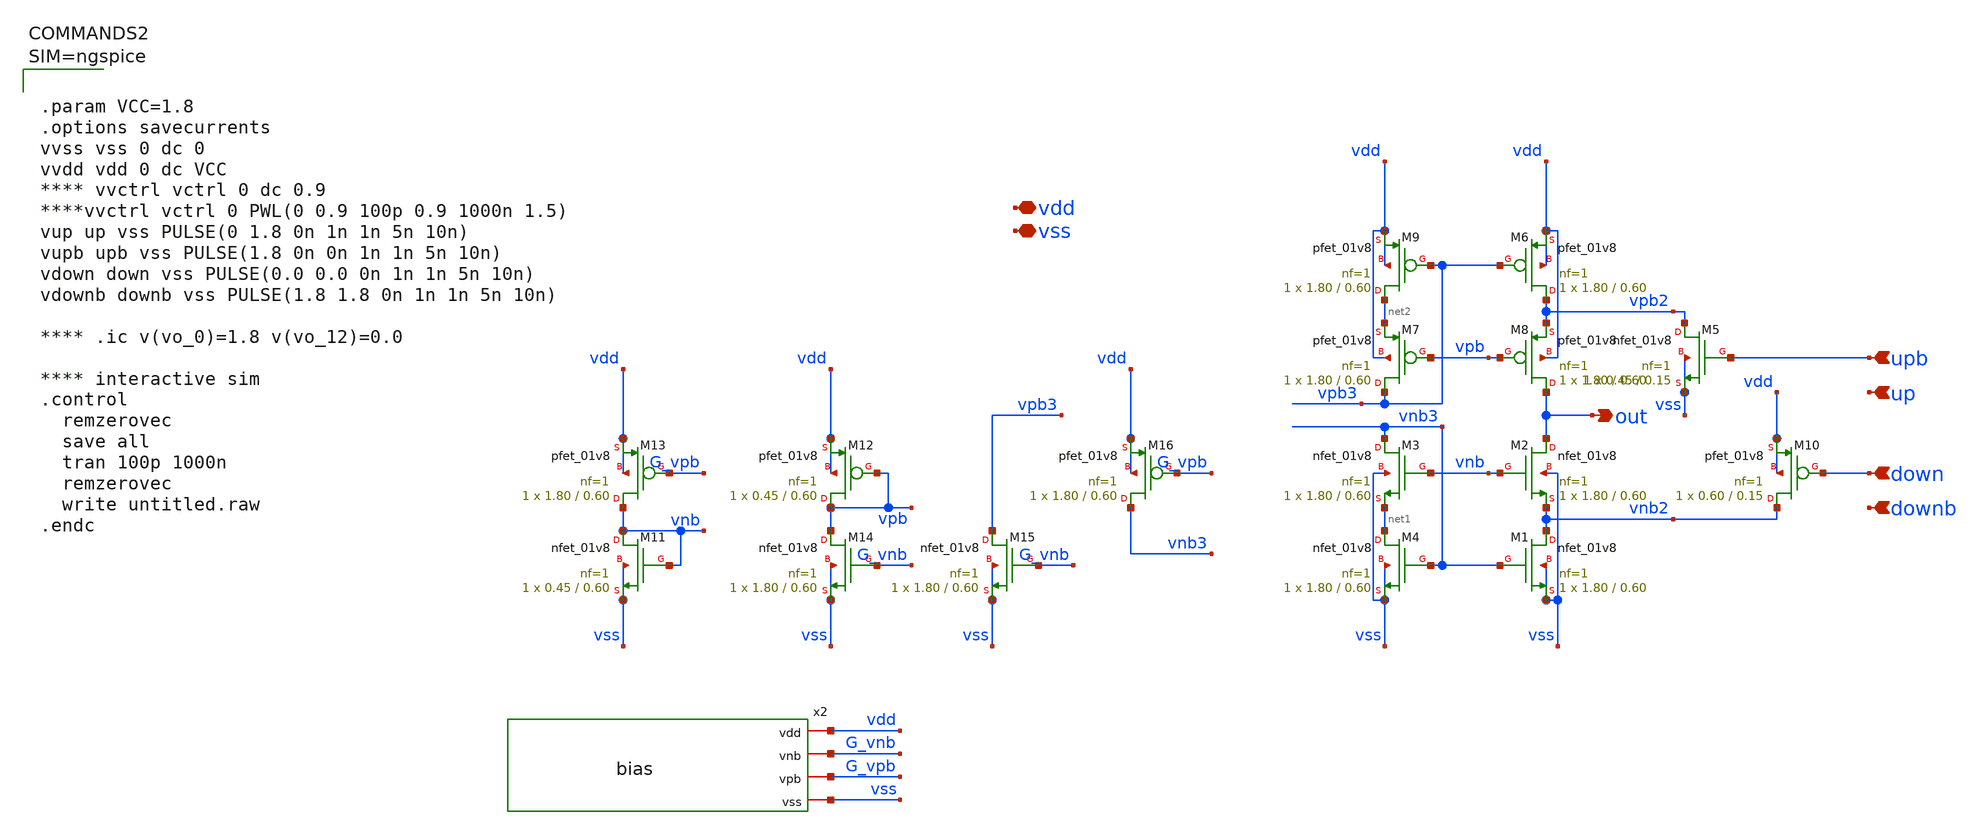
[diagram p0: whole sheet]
** sch_path: custom_gds/tt_um_mickey_pll/xschem/cp7.sch
.lib $::SKYWATER_MODELS/sky130.lib.spice tt
.include $::SKYWATER_STDCELLS/sky130_fd_sc_hd.spice

**.subckt cp7 upb up down downb out vdd vss
*.ipin upb
*.ipin up
*.ipin down
*.ipin downb
*.opin out
*.iopin vdd
*.iopin vss
XM1 vnb2 vnb3 vss vss sky130_fd_pr__nfet_01v8 L=0.60 W=1.80 nf=1 ad='int((nf+1)/2) * W/nf * 0.29' as='int((nf+2)/2) * W/nf * 0.29'
+ pd='2*int((nf+1)/2) * (W/nf + 0.29)' ps='2*int((nf+2)/2) * (W/nf + 0.29)' nrd='0.29 / W' nrs='0.29 / W'
+ sa=0 sb=0 sd=0 mult=1 m=1
XM2 out vnb vnb2 vss sky130_fd_pr__nfet_01v8 L=0.60 W=1.80 nf=1 ad='int((nf+1)/2) * W/nf * 0.29' as='int((nf+2)/2) * W/nf * 0.29'
+ pd='2*int((nf+1)/2) * (W/nf + 0.29)' ps='2*int((nf+2)/2) * (W/nf + 0.29)' nrd='0.29 / W' nrs='0.29 / W'
+ sa=0 sb=0 sd=0 mult=1 m=1
XM3 vnb3 vnb net1 vss sky130_fd_pr__nfet_01v8 L=0.60 W=1.80 nf=1 ad='int((nf+1)/2) * W/nf * 0.29' as='int((nf+2)/2) * W/nf * 0.29'
+ pd='2*int((nf+1)/2) * (W/nf + 0.29)' ps='2*int((nf+2)/2) * (W/nf + 0.29)' nrd='0.29 / W' nrs='0.29 / W'
+ sa=0 sb=0 sd=0 mult=1 m=1
XM4 net1 vnb3 vss vss sky130_fd_pr__nfet_01v8 L=0.60 W=1.80 nf=1 ad='int((nf+1)/2) * W/nf * 0.29' as='int((nf+2)/2) * W/nf * 0.29'
+ pd='2*int((nf+1)/2) * (W/nf + 0.29)' ps='2*int((nf+2)/2) * (W/nf + 0.29)' nrd='0.29 / W' nrs='0.29 / W'
+ sa=0 sb=0 sd=0 mult=1 m=1
XM5 vpb2 upb vss vss sky130_fd_pr__nfet_01v8 L=0.15 W=0.45 nf=1 ad='int((nf+1)/2) * W/nf * 0.29' as='int((nf+2)/2) * W/nf * 0.29'
+ pd='2*int((nf+1)/2) * (W/nf + 0.29)' ps='2*int((nf+2)/2) * (W/nf + 0.29)' nrd='0.29 / W' nrs='0.29 / W'
+ sa=0 sb=0 sd=0 mult=1 m=1
XM8 out vpb vpb2 vdd sky130_fd_pr__pfet_01v8 L=0.60 W=1.80 nf=1 ad='int((nf+1)/2) * W/nf * 0.29' as='int((nf+2)/2) * W/nf * 0.29'
+ pd='2*int((nf+1)/2) * (W/nf + 0.29)' ps='2*int((nf+2)/2) * (W/nf + 0.29)' nrd='0.29 / W' nrs='0.29 / W'
+ sa=0 sb=0 sd=0 mult=1 m=1
XM6 vpb2 vpb3 vdd vdd sky130_fd_pr__pfet_01v8 L=0.60 W=1.80 nf=1 ad='int((nf+1)/2) * W/nf * 0.29' as='int((nf+2)/2) * W/nf * 0.29'
+ pd='2*int((nf+1)/2) * (W/nf + 0.29)' ps='2*int((nf+2)/2) * (W/nf + 0.29)' nrd='0.29 / W' nrs='0.29 / W'
+ sa=0 sb=0 sd=0 mult=1 m=1
XM7 vpb3 vpb net2 vdd sky130_fd_pr__pfet_01v8 L=0.60 W=1.80 nf=1 ad='int((nf+1)/2) * W/nf * 0.29' as='int((nf+2)/2) * W/nf * 0.29'
+ pd='2*int((nf+1)/2) * (W/nf + 0.29)' ps='2*int((nf+2)/2) * (W/nf + 0.29)' nrd='0.29 / W' nrs='0.29 / W'
+ sa=0 sb=0 sd=0 mult=1 m=1
XM9 net2 vpb3 vdd vdd sky130_fd_pr__pfet_01v8 L=0.60 W=1.80 nf=1 ad='int((nf+1)/2) * W/nf * 0.29' as='int((nf+2)/2) * W/nf * 0.29'
+ pd='2*int((nf+1)/2) * (W/nf + 0.29)' ps='2*int((nf+2)/2) * (W/nf + 0.29)' nrd='0.29 / W' nrs='0.29 / W'
+ sa=0 sb=0 sd=0 mult=1 m=1
XM10 vnb2 down vdd vdd sky130_fd_pr__pfet_01v8 L=0.15 W=0.60 nf=1 ad='int((nf+1)/2) * W/nf * 0.29' as='int((nf+2)/2) * W/nf * 0.29'
+ pd='2*int((nf+1)/2) * (W/nf + 0.29)' ps='2*int((nf+2)/2) * (W/nf + 0.29)' nrd='0.29 / W' nrs='0.29 / W'
+ sa=0 sb=0 sd=0 mult=1 m=1
XM11 vnb vnb vss vss sky130_fd_pr__nfet_01v8 L=0.60 W=0.45 nf=1 ad='int((nf+1)/2) * W/nf * 0.29' as='int((nf+2)/2) * W/nf * 0.29'
+ pd='2*int((nf+1)/2) * (W/nf + 0.29)' ps='2*int((nf+2)/2) * (W/nf + 0.29)' nrd='0.29 / W' nrs='0.29 / W'
+ sa=0 sb=0 sd=0 mult=1 m=1
XM12 vpb vpb vdd vdd sky130_fd_pr__pfet_01v8 L=0.60 W=0.45 nf=1 ad='int((nf+1)/2) * W/nf * 0.29' as='int((nf+2)/2) * W/nf * 0.29'
+ pd='2*int((nf+1)/2) * (W/nf + 0.29)' ps='2*int((nf+2)/2) * (W/nf + 0.29)' nrd='0.29 / W' nrs='0.29 / W'
+ sa=0 sb=0 sd=0 mult=1 m=1
x2 vdd G_vnb G_vpb vss bias
XM13 vnb G_vpb vdd vdd sky130_fd_pr__pfet_01v8 L=0.60 W=1.80 nf=1 ad='int((nf+1)/2) * W/nf * 0.29' as='int((nf+2)/2) * W/nf * 0.29'
+ pd='2*int((nf+1)/2) * (W/nf + 0.29)' ps='2*int((nf+2)/2) * (W/nf + 0.29)' nrd='0.29 / W' nrs='0.29 / W'
+ sa=0 sb=0 sd=0 mult=1 m=1
XM14 vpb G_vnb vss vss sky130_fd_pr__nfet_01v8 L=0.60 W=1.80 nf=1 ad='int((nf+1)/2) * W/nf * 0.29' as='int((nf+2)/2) * W/nf * 0.29'
+ pd='2*int((nf+1)/2) * (W/nf + 0.29)' ps='2*int((nf+2)/2) * (W/nf + 0.29)' nrd='0.29 / W' nrs='0.29 / W'
+ sa=0 sb=0 sd=0 mult=1 m=1
XM15 vpb3 G_vnb vss vss sky130_fd_pr__nfet_01v8 L=0.60 W=1.80 nf=1 ad='int((nf+1)/2) * W/nf * 0.29' as='int((nf+2)/2) * W/nf * 0.29'
+ pd='2*int((nf+1)/2) * (W/nf + 0.29)' ps='2*int((nf+2)/2) * (W/nf + 0.29)' nrd='0.29 / W' nrs='0.29 / W'
+ sa=0 sb=0 sd=0 mult=1 m=1
XM16 vnb3 G_vpb vdd vdd sky130_fd_pr__pfet_01v8 L=0.60 W=1.80 nf=1 ad='int((nf+1)/2) * W/nf * 0.29' as='int((nf+2)/2) * W/nf * 0.29'
+ pd='2*int((nf+1)/2) * (W/nf + 0.29)' ps='2*int((nf+2)/2) * (W/nf + 0.29)' nrd='0.29 / W' nrs='0.29 / W'
+ sa=0 sb=0 sd=0 mult=1 m=1
**** begin user architecture code



.param VCC=1.8
.options savecurrents
vvss vss 0 dc 0
vvdd vdd 0 dc VCC
**** vvctrl vctrl 0 dc 0.9
****vvctrl vctrl 0 PWL(0 0.9 100p 0.9 1000n 1.5)
vup up vss PULSE(0 1.8 0n 1n 1n 5n 10n)
vupb upb vss PULSE(1.8 0n 0n 1n 1n 5n 10n)
vdown down vss PULSE(0.0 0.0 0n 1n 1n 5n 10n)
vdownb downb vss PULSE(1.8 1.8 0n 1n 1n 5n 10n)

**** .ic v(vo_0)=1.8 v(vo_12)=0.0

**** interactive sim
.control
  remzerovec
  save all
  tran 100p 1000n
  remzerovec
  write untitled.raw
.endc



**** end user architecture code
**.ends

* expanding   symbol:  bias.sym # of pins=4
** sym_path: custom_gds/tt_um_mickey_pll/xschem/bias.sym
** sch_path: custom_gds/tt_um_mickey_pll/xschem/bias.sch
.subckt bias vdd vnb vpb vss
*.iopin vdd
*.iopin vss
*.iopin vnb
*.iopin vpb
XM1 vpb vnb vss vss sky130_fd_pr__nfet_01v8 L=0.60 W=1.80 nf=1 ad='int((nf+1)/2) * W/nf * 0.29' as='int((nf+2)/2) * W/nf * 0.29'
+ pd='2*int((nf+1)/2) * (W/nf + 0.29)' ps='2*int((nf+2)/2) * (W/nf + 0.29)' nrd='0.29 / W' nrs='0.29 / W'
+ sa=0 sb=0 sd=0 mult=1 m=1
XM2 vnb vnb vss vss sky130_fd_pr__nfet_01v8 L=0.60 W=1.80 nf=1 ad='int((nf+1)/2) * W/nf * 0.29' as='int((nf+2)/2) * W/nf * 0.29'
+ pd='2*int((nf+1)/2) * (W/nf + 0.29)' ps='2*int((nf+2)/2) * (W/nf + 0.29)' nrd='0.29 / W' nrs='0.29 / W'
+ sa=0 sb=0 sd=0 mult=1 m=1
XM3 vpb vpb vdd vdd sky130_fd_pr__pfet_01v8 L=0.60 W=1.80 nf=1 ad='int((nf+1)/2) * W/nf * 0.29' as='int((nf+2)/2) * W/nf * 0.29'
+ pd='2*int((nf+1)/2) * (W/nf + 0.29)' ps='2*int((nf+2)/2) * (W/nf + 0.29)' nrd='0.29 / W' nrs='0.29 / W'
+ sa=0 sb=0 sd=0 mult=1 m=1
XM4 vnb vpb net1 vdd sky130_fd_pr__pfet_01v8 L=0.60 W=7.20 nf=4 ad='int((nf+1)/2) * W/nf * 0.29' as='int((nf+2)/2) * W/nf * 0.29'
+ pd='2*int((nf+1)/2) * (W/nf + 0.29)' ps='2*int((nf+2)/2) * (W/nf + 0.29)' nrd='0.29 / W' nrs='0.29 / W'
+ sa=0 sb=0 sd=0 mult=1 m=1
XM5 net2 vpb vdd vdd sky130_fd_pr__pfet_01v8 L=0.60 W=1.80 nf=1 ad='int((nf+1)/2) * W/nf * 0.29' as='int((nf+2)/2) * W/nf * 0.29'
+ pd='2*int((nf+1)/2) * (W/nf + 0.29)' ps='2*int((nf+2)/2) * (W/nf + 0.29)' nrd='0.29 / W' nrs='0.29 / W'
+ sa=0 sb=0 sd=0 mult=1 m=1
XM6 net2 net2 vss vss sky130_fd_pr__nfet_01v8 L=1.50 W=0.45 nf=1 ad='int((nf+1)/2) * W/nf * 0.29' as='int((nf+2)/2) * W/nf * 0.29'
+ pd='2*int((nf+1)/2) * (W/nf + 0.29)' ps='2*int((nf+2)/2) * (W/nf + 0.29)' nrd='0.29 / W' nrs='0.29 / W'
+ sa=0 sb=0 sd=0 mult=1 m=1
XM7 vnb net2 vpb vdd sky130_fd_pr__pfet_01v8 L=0.60 W=0.9 nf=1 ad='int((nf+1)/2) * W/nf * 0.29' as='int((nf+2)/2) * W/nf * 0.29'
+ pd='2*int((nf+1)/2) * (W/nf + 0.29)' ps='2*int((nf+2)/2) * (W/nf + 0.29)' nrd='0.29 / W' nrs='0.29 / W'
+ sa=0 sb=0 sd=0 mult=1 m=1
XR1 net1 vdd vdd sky130_fd_pr__res_xhigh_po_0p35 L=2.000 mult=1 m=1
.ends

.end
